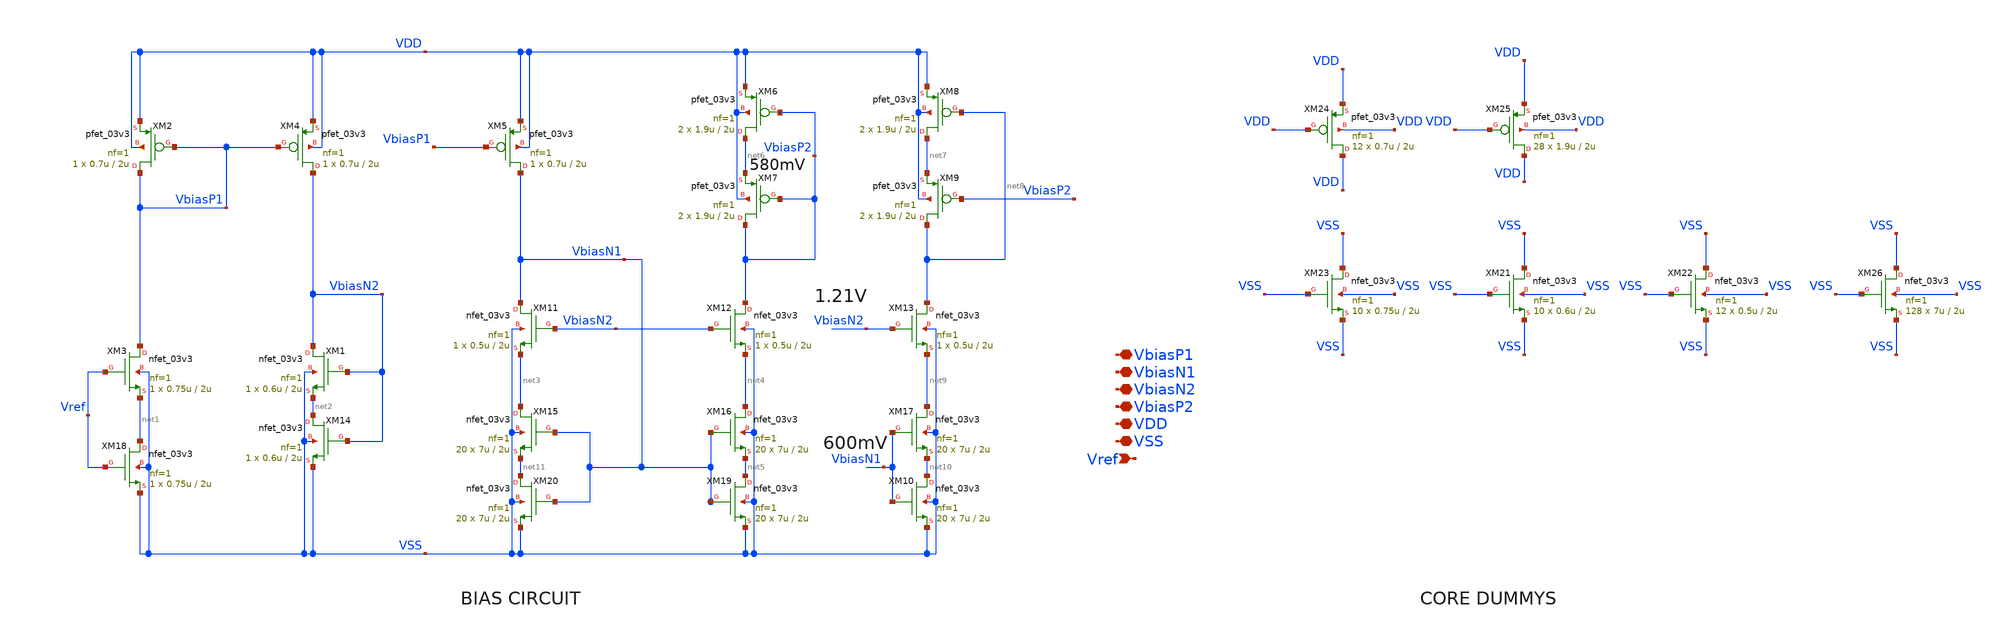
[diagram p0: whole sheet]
** sch_path: designs/gf180/error_amplifier_N_input_bias_v2/xschem/error_amplifier_N_input_bias_v2.sch
**.subckt error_amplifier_N_input_bias_v2 Vref VbiasN1 VbiasN2 VDD VbiasP2 VSS VbiasP1
*.ipin Vref
*.iopin VbiasN1
*.iopin VbiasN2
*.iopin VDD
*.iopin VbiasP2
*.iopin VSS
*.iopin VbiasP1
XM1 VbiasN2 VbiasN2 net2 VSS nfet_03v3 L=2u W=0.6u nf=1 ad='int((nf+1)/2) * W/nf * 0.18u' as='int((nf+2)/2) * W/nf * 0.18u'
+ pd='2*int((nf+1)/2) * (W/nf + 0.18u)' ps='2*int((nf+2)/2) * (W/nf + 0.18u)' nrd='0.18u / W' nrs='0.18u / W'
+ sa=0 sb=0 sd=0 m=1
XM2 VbiasP1 VbiasP1 VDD VDD pfet_03v3 L=2u W=0.7u nf=1 ad='int((nf+1)/2) * W/nf * 0.18u' as='int((nf+2)/2) * W/nf * 0.18u'
+ pd='2*int((nf+1)/2) * (W/nf + 0.18u)' ps='2*int((nf+2)/2) * (W/nf + 0.18u)' nrd='0.18u / W' nrs='0.18u / W'
+ sa=0 sb=0 sd=0 m=1
XM3 VbiasP1 Vref net1 VSS nfet_03v3 L=2u W=0.75u nf=1 ad='int((nf+1)/2) * W/nf * 0.18u' as='int((nf+2)/2) * W/nf * 0.18u'
+ pd='2*int((nf+1)/2) * (W/nf + 0.18u)' ps='2*int((nf+2)/2) * (W/nf + 0.18u)' nrd='0.18u / W' nrs='0.18u / W'
+ sa=0 sb=0 sd=0 m=1
XM4 VbiasN2 VbiasP1 VDD VDD pfet_03v3 L=2u W=0.7u nf=1 ad='int((nf+1)/2) * W/nf * 0.18u' as='int((nf+2)/2) * W/nf * 0.18u'
+ pd='2*int((nf+1)/2) * (W/nf + 0.18u)' ps='2*int((nf+2)/2) * (W/nf + 0.18u)' nrd='0.18u / W' nrs='0.18u / W'
+ sa=0 sb=0 sd=0 m=1
XM5 VbiasN1 VbiasP1 VDD VDD pfet_03v3 L=2u W=0.7u nf=1 ad='int((nf+1)/2) * W/nf * 0.18u' as='int((nf+2)/2) * W/nf * 0.18u'
+ pd='2*int((nf+1)/2) * (W/nf + 0.18u)' ps='2*int((nf+2)/2) * (W/nf + 0.18u)' nrd='0.18u / W' nrs='0.18u / W'
+ sa=0 sb=0 sd=0 m=1
XM6 net6 VbiasP2 VDD VDD pfet_03v3 L=2u W=1.9u nf=1 ad='int((nf+1)/2) * W/nf * 0.18u' as='int((nf+2)/2) * W/nf * 0.18u'
+ pd='2*int((nf+1)/2) * (W/nf + 0.18u)' ps='2*int((nf+2)/2) * (W/nf + 0.18u)' nrd='0.18u / W' nrs='0.18u / W'
+ sa=0 sb=0 sd=0 m=2
XM7 VbiasP2 VbiasP2 net6 VDD pfet_03v3 L=2u W=1.9u nf=1 ad='int((nf+1)/2) * W/nf * 0.18u' as='int((nf+2)/2) * W/nf * 0.18u'
+ pd='2*int((nf+1)/2) * (W/nf + 0.18u)' ps='2*int((nf+2)/2) * (W/nf + 0.18u)' nrd='0.18u / W' nrs='0.18u / W'
+ sa=0 sb=0 sd=0 m=2
XM8 net7 net8 VDD VDD pfet_03v3 L=2u W=1.9u nf=1 ad='int((nf+1)/2) * W/nf * 0.18u' as='int((nf+2)/2) * W/nf * 0.18u'
+ pd='2*int((nf+1)/2) * (W/nf + 0.18u)' ps='2*int((nf+2)/2) * (W/nf + 0.18u)' nrd='0.18u / W' nrs='0.18u / W'
+ sa=0 sb=0 sd=0 m=2
XM9 net8 VbiasP2 net7 VDD pfet_03v3 L=2u W=1.9u nf=1 ad='int((nf+1)/2) * W/nf * 0.18u' as='int((nf+2)/2) * W/nf * 0.18u'
+ pd='2*int((nf+1)/2) * (W/nf + 0.18u)' ps='2*int((nf+2)/2) * (W/nf + 0.18u)' nrd='0.18u / W' nrs='0.18u / W'
+ sa=0 sb=0 sd=0 m=2
XM10 net10 VbiasN1 VSS VSS nfet_03v3 L=2u W=7u nf=1 ad='int((nf+1)/2) * W/nf * 0.18u' as='int((nf+2)/2) * W/nf * 0.18u'
+ pd='2*int((nf+1)/2) * (W/nf + 0.18u)' ps='2*int((nf+2)/2) * (W/nf + 0.18u)' nrd='0.18u / W' nrs='0.18u / W'
+ sa=0 sb=0 sd=0 m=20
XM11 VbiasN1 VbiasN2 net3 VSS nfet_03v3 L=2u W=0.5u nf=1 ad='int((nf+1)/2) * W/nf * 0.18u' as='int((nf+2)/2) * W/nf * 0.18u'
+ pd='2*int((nf+1)/2) * (W/nf + 0.18u)' ps='2*int((nf+2)/2) * (W/nf + 0.18u)' nrd='0.18u / W' nrs='0.18u / W'
+ sa=0 sb=0 sd=0 m=1
XM12 VbiasP2 VbiasN2 net4 VSS nfet_03v3 L=2u W=0.5u nf=1 ad='int((nf+1)/2) * W/nf * 0.18u' as='int((nf+2)/2) * W/nf * 0.18u'
+ pd='2*int((nf+1)/2) * (W/nf + 0.18u)' ps='2*int((nf+2)/2) * (W/nf + 0.18u)' nrd='0.18u / W' nrs='0.18u / W'
+ sa=0 sb=0 sd=0 m=1
XM13 net8 VbiasN2 net9 VSS nfet_03v3 L=2u W=0.5u nf=1 ad='int((nf+1)/2) * W/nf * 0.18u' as='int((nf+2)/2) * W/nf * 0.18u'
+ pd='2*int((nf+1)/2) * (W/nf + 0.18u)' ps='2*int((nf+2)/2) * (W/nf + 0.18u)' nrd='0.18u / W' nrs='0.18u / W'
+ sa=0 sb=0 sd=0 m=1
XM14 net2 VbiasN2 VSS VSS nfet_03v3 L=2u W=0.6u nf=1 ad='int((nf+1)/2) * W/nf * 0.18u' as='int((nf+2)/2) * W/nf * 0.18u'
+ pd='2*int((nf+1)/2) * (W/nf + 0.18u)' ps='2*int((nf+2)/2) * (W/nf + 0.18u)' nrd='0.18u / W' nrs='0.18u / W'
+ sa=0 sb=0 sd=0 m=1
XM15 net3 VbiasN1 net11 VSS nfet_03v3 L=2u W=7u nf=1 ad='int((nf+1)/2) * W/nf * 0.18u' as='int((nf+2)/2) * W/nf * 0.18u'
+ pd='2*int((nf+1)/2) * (W/nf + 0.18u)' ps='2*int((nf+2)/2) * (W/nf + 0.18u)' nrd='0.18u / W' nrs='0.18u / W'
+ sa=0 sb=0 sd=0 m=20
XM16 net4 VbiasN1 net5 VSS nfet_03v3 L=2u W=7u nf=1 ad='int((nf+1)/2) * W/nf * 0.18u' as='int((nf+2)/2) * W/nf * 0.18u'
+ pd='2*int((nf+1)/2) * (W/nf + 0.18u)' ps='2*int((nf+2)/2) * (W/nf + 0.18u)' nrd='0.18u / W' nrs='0.18u / W'
+ sa=0 sb=0 sd=0 m=20
XM17 net9 VbiasN1 net10 VSS nfet_03v3 L=2u W=7u nf=1 ad='int((nf+1)/2) * W/nf * 0.18u' as='int((nf+2)/2) * W/nf * 0.18u'
+ pd='2*int((nf+1)/2) * (W/nf + 0.18u)' ps='2*int((nf+2)/2) * (W/nf + 0.18u)' nrd='0.18u / W' nrs='0.18u / W'
+ sa=0 sb=0 sd=0 m=20
XM18 net1 Vref VSS VSS nfet_03v3 L=2u W=0.75u nf=1 ad='int((nf+1)/2) * W/nf * 0.18u' as='int((nf+2)/2) * W/nf * 0.18u'
+ pd='2*int((nf+1)/2) * (W/nf + 0.18u)' ps='2*int((nf+2)/2) * (W/nf + 0.18u)' nrd='0.18u / W' nrs='0.18u / W'
+ sa=0 sb=0 sd=0 m=1
XM19 net5 VbiasN1 VSS VSS nfet_03v3 L=2u W=7u nf=1 ad='int((nf+1)/2) * W/nf * 0.18u' as='int((nf+2)/2) * W/nf * 0.18u'
+ pd='2*int((nf+1)/2) * (W/nf + 0.18u)' ps='2*int((nf+2)/2) * (W/nf + 0.18u)' nrd='0.18u / W' nrs='0.18u / W'
+ sa=0 sb=0 sd=0 m=20
XM20 net11 VbiasN1 VSS VSS nfet_03v3 L=2u W=7u nf=1 ad='int((nf+1)/2) * W/nf * 0.18u' as='int((nf+2)/2) * W/nf * 0.18u'
+ pd='2*int((nf+1)/2) * (W/nf + 0.18u)' ps='2*int((nf+2)/2) * (W/nf + 0.18u)' nrd='0.18u / W' nrs='0.18u / W'
+ sa=0 sb=0 sd=0 m=20
XM21 VSS VSS VSS VSS nfet_03v3 L=2u W=0.6u nf=1 ad='int((nf+1)/2) * W/nf * 0.18u' as='int((nf+2)/2) * W/nf * 0.18u'
+ pd='2*int((nf+1)/2) * (W/nf + 0.18u)' ps='2*int((nf+2)/2) * (W/nf + 0.18u)' nrd='0.18u / W' nrs='0.18u / W'
+ sa=0 sb=0 sd=0 m=10
XM22 VSS VSS VSS VSS nfet_03v3 L=2u W=0.5u nf=1 ad='int((nf+1)/2) * W/nf * 0.18u' as='int((nf+2)/2) * W/nf * 0.18u'
+ pd='2*int((nf+1)/2) * (W/nf + 0.18u)' ps='2*int((nf+2)/2) * (W/nf + 0.18u)' nrd='0.18u / W' nrs='0.18u / W'
+ sa=0 sb=0 sd=0 m=12
XM23 VSS VSS VSS VSS nfet_03v3 L=2u W=0.75u nf=1 ad='int((nf+1)/2) * W/nf * 0.18u' as='int((nf+2)/2) * W/nf * 0.18u'
+ pd='2*int((nf+1)/2) * (W/nf + 0.18u)' ps='2*int((nf+2)/2) * (W/nf + 0.18u)' nrd='0.18u / W' nrs='0.18u / W'
+ sa=0 sb=0 sd=0 m=10
XM24 VDD VDD VDD VDD pfet_03v3 L=2u W=0.7u nf=1 ad='int((nf+1)/2) * W/nf * 0.18u' as='int((nf+2)/2) * W/nf * 0.18u'
+ pd='2*int((nf+1)/2) * (W/nf + 0.18u)' ps='2*int((nf+2)/2) * (W/nf + 0.18u)' nrd='0.18u / W' nrs='0.18u / W'
+ sa=0 sb=0 sd=0 m=12
XM25 VDD VDD VDD VDD pfet_03v3 L=2u W=1.9u nf=1 ad='int((nf+1)/2) * W/nf * 0.18u' as='int((nf+2)/2) * W/nf * 0.18u'
+ pd='2*int((nf+1)/2) * (W/nf + 0.18u)' ps='2*int((nf+2)/2) * (W/nf + 0.18u)' nrd='0.18u / W' nrs='0.18u / W'
+ sa=0 sb=0 sd=0 m=28
XM26 VSS VSS VSS VSS nfet_03v3 L=2u W=7u nf=1 ad='int((nf+1)/2) * W/nf * 0.18u' as='int((nf+2)/2) * W/nf * 0.18u'
+ pd='2*int((nf+1)/2) * (W/nf + 0.18u)' ps='2*int((nf+2)/2) * (W/nf + 0.18u)' nrd='0.18u / W' nrs='0.18u / W'
+ sa=0 sb=0 sd=0 m=128
**.ends
.end
